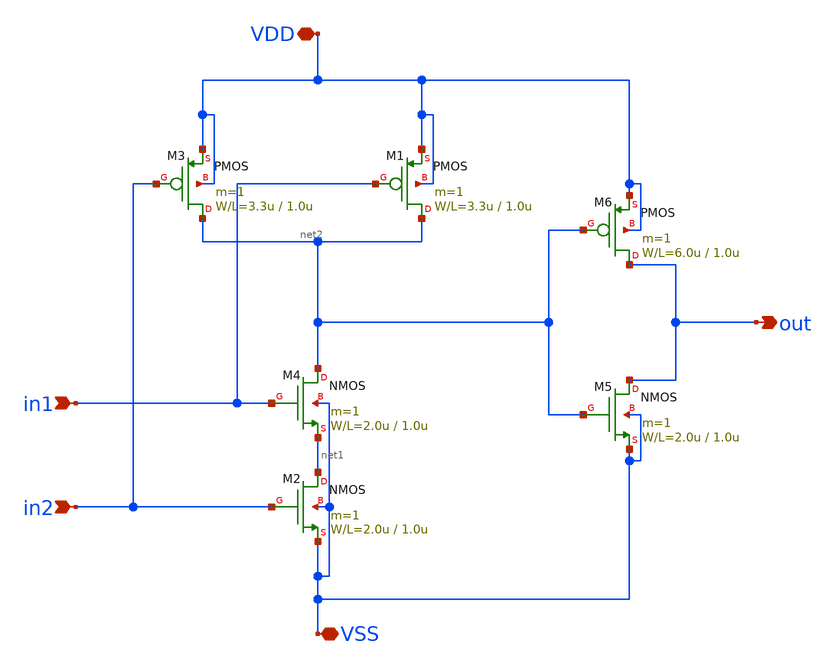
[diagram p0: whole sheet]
** sch_path: member_project/SaltyChip703/AND_circuit/and.sch
**.subckt and in1 VDD VSS in2 out
*.ipin in1
*.iopin VDD
*.iopin VSS
*.ipin in2
*.opin out
M2 net1 in2 VSS VSS NMOS L=1.0u W=2.0u m=1
M1 net2 in1 VDD VDD PMOS L=1.0u W=3.3u m=1
M3 net2 in2 VDD VDD PMOS L=1.0u W=3.3u m=1
M4 net2 in1 net1 VSS NMOS L=1.0u W=2.0u m=1
M5 out net2 VSS VSS NMOS L=1.0u W=2.0u m=1
M6 out net2 VDD VDD PMOS L=1.0u W=6.0u m=1
**.ends
.end
